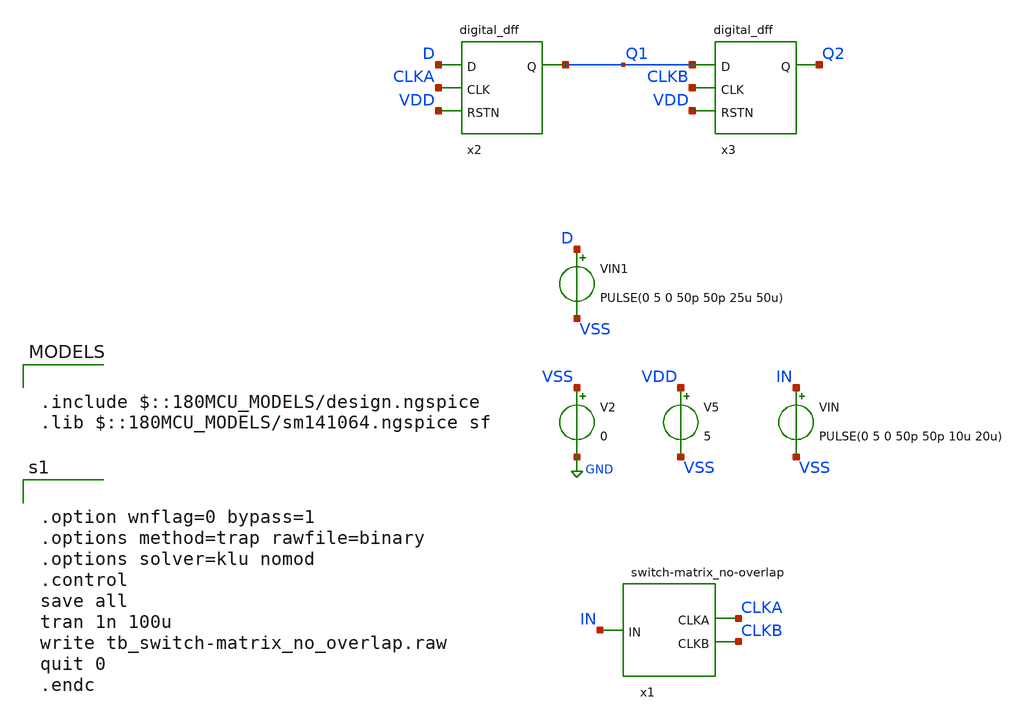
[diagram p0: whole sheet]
** sch_path: designs/libs/tb_analog/tb_switch-matrix/tb_switch-matrix_no_overlap.sch
**.subckt tb_switch-matrix_no_overlap
x1 IN VSS VDD CLKA CLKB switch-matrix_no-overlap
V2 VSS GND 0
V5 VDD VSS 5
VIN IN VSS PULSE(0 5 0 50p 50p 10u 20u)
x2 D CLKA VDD VSS VDD Q1 digital_dff
x3 Q1 CLKB VDD VSS VDD Q2 digital_dff
VIN1 D VSS PULSE(0 5 0 50p 50p 25u 50u)
**** begin user architecture code

.include $::180MCU_MODELS/design.ngspice
.lib $::180MCU_MODELS/sm141064.ngspice sf



.option wnflag=0 bypass=1
.options method=trap rawfile=binary
.options solver=klu nomod
.control
save all
tran 1n 100u
write tb_switch-matrix_no_overlap.raw
quit 0
.endc


**** end user architecture code
**.ends
.GLOBAL GND
.end
